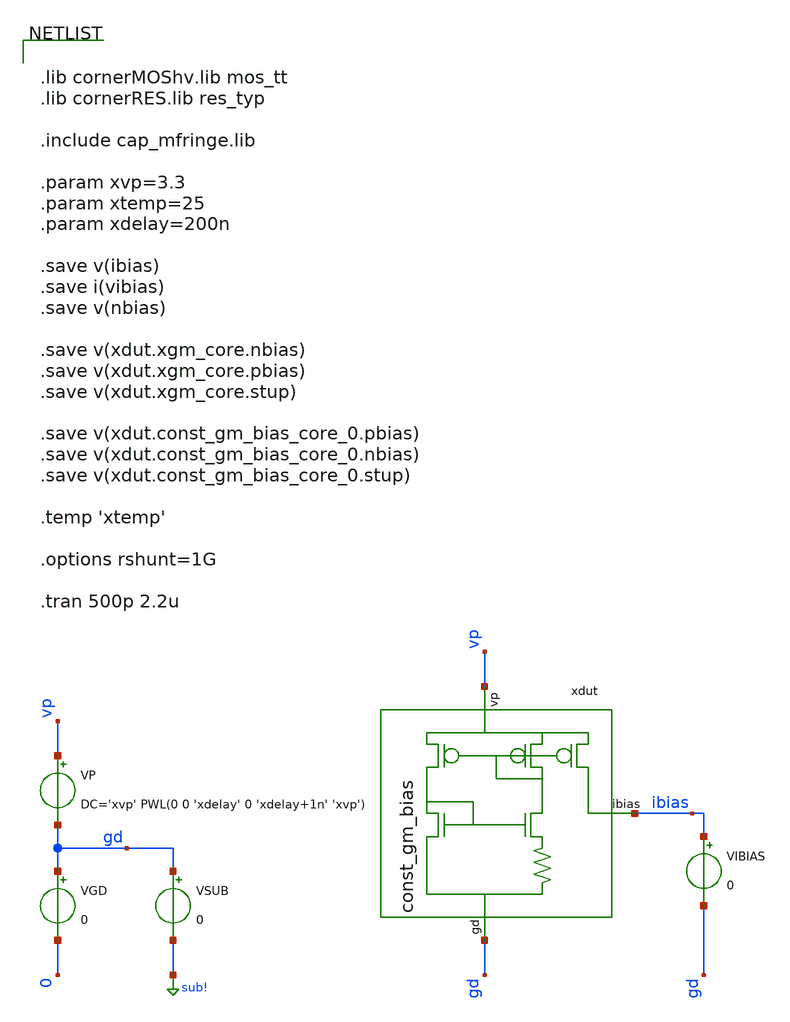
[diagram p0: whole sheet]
** sch_path: testbench/const_gm_bias_startup_tb.sch
**.subckt const_gm_bias_startup_tb
VP vp gd DC='xvp' PWL(0 0 'xdelay' 0 'xdelay+1n' 'xvp')
VGD gd 0 0
VSUB gd sub! 0
xdut vp ibias gd const_gm_bias
VIBIAS ibias gd 0
**** begin user architecture code


.lib cornerMOShv.lib mos_tt
.lib cornerRES.lib res_typ

.include cap_mfringe.lib

.param xvp=3.3
.param xtemp=25
.param xdelay=200n

.save v(ibias)
.save i(vibias)
.save v(nbias)

.save v(xdut.xgm_core.nbias)
.save v(xdut.xgm_core.pbias)
.save v(xdut.xgm_core.stup)

.save v(xdut.const_gm_bias_core_0.pbias)
.save v(xdut.const_gm_bias_core_0.nbias)
.save v(xdut.const_gm_bias_core_0.stup)

.temp 'xtemp'

.options rshunt=1G

.tran 500p 2.2u


**** end user architecture code
**.ends
.GLOBAL sub!
.end
